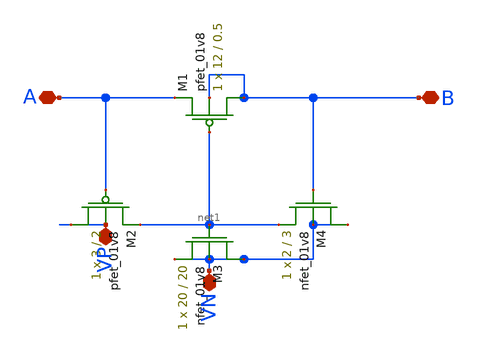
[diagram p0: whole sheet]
** sch_path: schematic/memristor_emulator.sch
**.subckt memristor_emulator VN VP B A
*.iopin VN
*.iopin VP
*.iopin B
*.iopin A
XM1 B net1 A B sky130_fd_pr__pfet_01v8 L=0.5 W=12 nf=1 ad='int((nf+1)/2) * W/nf * 0.29' as='int((nf+2)/2) * W/nf * 0.29'
+ pd='2*int((nf+1)/2) * (W/nf + 0.29)' ps='2*int((nf+2)/2) * (W/nf + 0.29)' nrd='0.29 / W' nrs='0.29 / W'
+ sa=0 sb=0 sd=0 mult=1 m=1
XM2 VP A net1 VP sky130_fd_pr__pfet_01v8 L=2 W=3 nf=1 ad='int((nf+1)/2) * W/nf * 0.29' as='int((nf+2)/2) * W/nf * 0.29'
+ pd='2*int((nf+1)/2) * (W/nf + 0.29)' ps='2*int((nf+2)/2) * (W/nf + 0.29)' nrd='0.29 / W' nrs='0.29 / W'
+ sa=0 sb=0 sd=0 mult=1 m=1
XM3 VN net1 VN VN sky130_fd_pr__nfet_01v8 L=20 W=20 nf=1 ad='int((nf+1)/2) * W/nf * 0.29' as='int((nf+2)/2) * W/nf * 0.29'
+ pd='2*int((nf+1)/2) * (W/nf + 0.29)' ps='2*int((nf+2)/2) * (W/nf + 0.29)' nrd='0.29 / W' nrs='0.29 / W'
+ sa=0 sb=0 sd=0 mult=1 m=1
XM4 VN B net1 VN sky130_fd_pr__nfet_01v8 L=3 W=2 nf=1 ad='int((nf+1)/2) * W/nf * 0.29' as='int((nf+2)/2) * W/nf * 0.29'
+ pd='2*int((nf+1)/2) * (W/nf + 0.29)' ps='2*int((nf+2)/2) * (W/nf + 0.29)' nrd='0.29 / W' nrs='0.29 / W'
+ sa=0 sb=0 sd=0 mult=1 m=1
**.ends
.end
